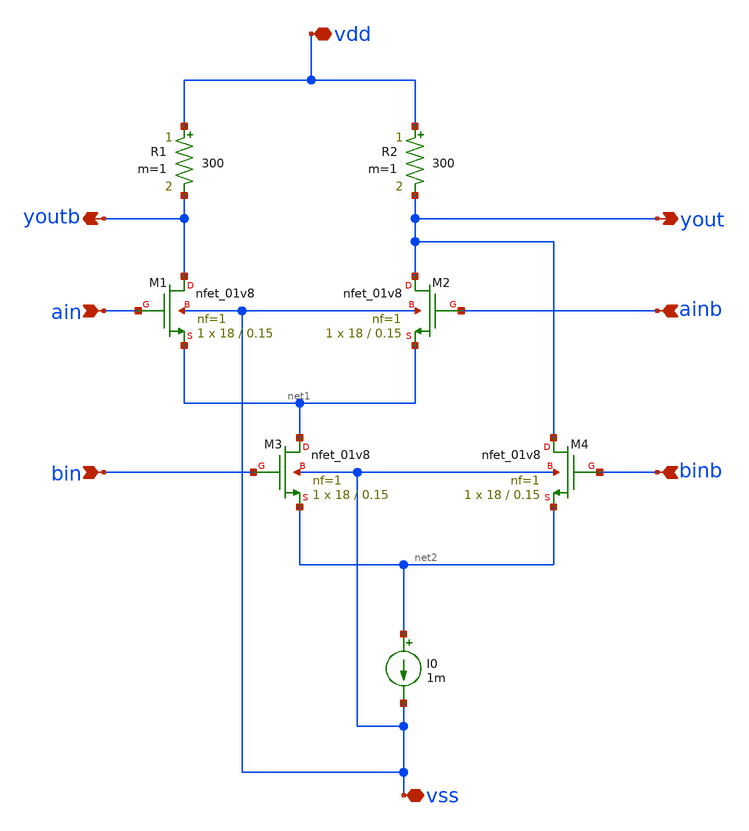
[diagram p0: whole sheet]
** sch_path: xschem/cml_and_or.sch
**.subckt cml_and_or ain ainb binb bin yout youtb vdd vss
*.ipin ain
*.ipin ainb
*.ipin binb
*.ipin bin
*.opin yout
*.opin youtb
*.iopin vdd
*.iopin vss
XM1 youtb ain net1 vss sky130_fd_pr__nfet_01v8 L=0.15 W=18 nf=1 ad='int((nf+1)/2) * W/nf * 0.29' as='int((nf+2)/2) * W/nf * 0.29'
+ pd='2*int((nf+1)/2) * (W/nf + 0.29)' ps='2*int((nf+2)/2) * (W/nf + 0.29)' nrd='0.29 / W' nrs='0.29 / W'
+ sa=0 sb=0 sd=0 mult=1 m=1
XM2 yout ainb net1 vss sky130_fd_pr__nfet_01v8 L=0.15 W=18 nf=1 ad='int((nf+1)/2) * W/nf * 0.29' as='int((nf+2)/2) * W/nf * 0.29'
+ pd='2*int((nf+1)/2) * (W/nf + 0.29)' ps='2*int((nf+2)/2) * (W/nf + 0.29)' nrd='0.29 / W' nrs='0.29 / W'
+ sa=0 sb=0 sd=0 mult=1 m=1
XM3 net1 bin net2 vss sky130_fd_pr__nfet_01v8 L=0.15 W=18 nf=1 ad='int((nf+1)/2) * W/nf * 0.29' as='int((nf+2)/2) * W/nf * 0.29'
+ pd='2*int((nf+1)/2) * (W/nf + 0.29)' ps='2*int((nf+2)/2) * (W/nf + 0.29)' nrd='0.29 / W' nrs='0.29 / W'
+ sa=0 sb=0 sd=0 mult=1 m=1
XM4 yout binb net2 vss sky130_fd_pr__nfet_01v8 L=0.15 W=18 nf=1 ad='int((nf+1)/2) * W/nf * 0.29' as='int((nf+2)/2) * W/nf * 0.29'
+ pd='2*int((nf+1)/2) * (W/nf + 0.29)' ps='2*int((nf+2)/2) * (W/nf + 0.29)' nrd='0.29 / W' nrs='0.29 / W'
+ sa=0 sb=0 sd=0 mult=1 m=1
R1 vdd youtb 300 m=1
R2 vdd yout 300 m=1
I0 net2 vss 1m
**.ends
.end
